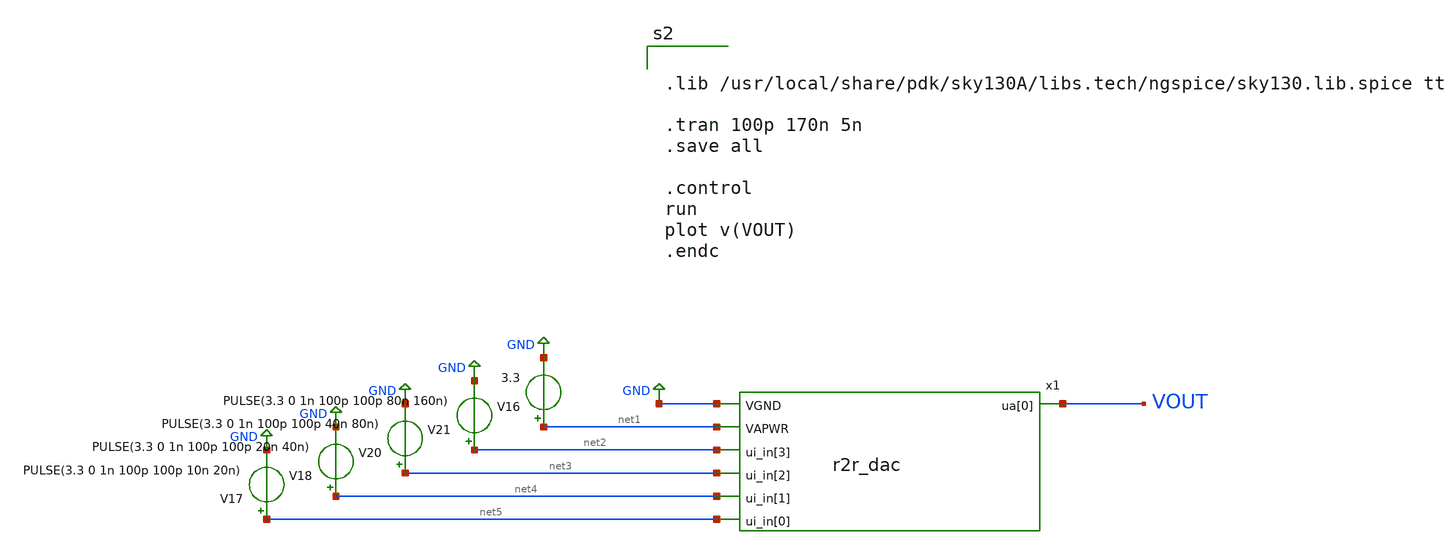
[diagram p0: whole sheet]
** sch_path: xschem/dac_tb.sch
**.subckt dac_tb
x1 VOUT GND net1 net2 net3 net4 net5 r2r_dac
V17 net5 GND PULSE(3.3 0 1n 100p 100p 10n 20n)
V18 net4 GND PULSE(3.3 0 1n 100p 100p 20n 40n)
V20 net3 GND PULSE(3.3 0 1n 100p 100p 40n 80n)
V21 net2 GND PULSE(3.3 0 1n 100p 100p 80n 160n)
V16 net1 GND 3.3
**** begin user architecture code


.lib /usr/local/share/pdk/sky130A/libs.tech/ngspice/sky130.lib.spice tt

.tran 100p 170n 5n
.save all

.control
run
plot v(VOUT)
.endc


**** end user architecture code
**.ends

* expanding   symbol:  /home/titus/TinyTapeout_R2R_DAC/xschem/r2r_dac.sym # of pins=7
** sym_path: xschem/r2r_dac.sym
** sch_path: xschem/r2r_dac.sch
.subckt r2r_dac ua[0] VGND VAPWR ui_in[3] ui_in[2] ui_in[1] ui_in[0]
*.opin ua[0]
*.ipin VGND
*.ipin ui_in[0]
*.ipin ui_in[1]
*.ipin ui_in[2]
*.ipin ui_in[3]
*.ipin VAPWR
XM10 net4 net5 VAPWR VAPWR sky130_fd_pr__pfet_g5v0d10v5 L=0.5 W=4 nf=1 ad=0 as=0 pd=0 ps=0 nrd=0
+ nrs=0 sa=0 sb=0 sd=0 mult=1 m=1
XM17 net4 ui_in[0] VGND VAPWR sky130_fd_pr__pfet_g5v0d10v5 L=0.5 W=4 nf=1 ad=0 as=0 pd=0 ps=0 nrd=0
+ nrs=0 sa=0 sb=0 sd=0 mult=1 m=1
XM26 net4 net5 VGND VGND sky130_fd_pr__nfet_g5v0d10v5 L=0.5 W=2 nf=1 ad=0 as=0 pd=0 ps=0 nrd=0 nrs=0
+ sa=0 sb=0 sd=0 mult=1 m=1
XM27 net4 ui_in[0] VAPWR VGND sky130_fd_pr__nfet_g5v0d10v5 L=0.5 W=2 nf=1 ad=0 as=0 pd=0 ps=0 nrd=0
+ nrs=0 sa=0 sb=0 sd=0 mult=1 m=1
XM32 net1 net6 VAPWR VAPWR sky130_fd_pr__pfet_g5v0d10v5 L=0.5 W=4 nf=1 ad=0 as=0 pd=0 ps=0 nrd=0
+ nrs=0 sa=0 sb=0 sd=0 mult=1 m=1
XM34 net1 ui_in[1] VGND VAPWR sky130_fd_pr__pfet_g5v0d10v5 L=0.5 W=4 nf=1 ad=0 as=0 pd=0 ps=0 nrd=0
+ nrs=0 sa=0 sb=0 sd=0 mult=1 m=1
XM1 net1 net6 VGND VGND sky130_fd_pr__nfet_g5v0d10v5 L=0.5 W=2 nf=1 ad=0 as=0 pd=0 ps=0 nrd=0 nrs=0
+ sa=0 sb=0 sd=0 mult=1 m=1
XM2 net1 ui_in[1] VAPWR VGND sky130_fd_pr__nfet_g5v0d10v5 L=0.5 W=2 nf=1 ad=0 as=0 pd=0 ps=0 nrd=0
+ nrs=0 sa=0 sb=0 sd=0 mult=1 m=1
XM4 net2 net7 VAPWR VAPWR sky130_fd_pr__pfet_g5v0d10v5 L=0.5 W=4 nf=1 ad=0 as=0 pd=0 ps=0 nrd=0
+ nrs=0 sa=0 sb=0 sd=0 mult=1 m=1
XM5 net2 ui_in[2] VGND VAPWR sky130_fd_pr__pfet_g5v0d10v5 L=0.5 W=4 nf=1 ad=0 as=0 pd=0 ps=0 nrd=0
+ nrs=0 sa=0 sb=0 sd=0 mult=1 m=1
XM8 net2 net7 VGND VGND sky130_fd_pr__nfet_g5v0d10v5 L=0.5 W=2 nf=1 ad=0 as=0 pd=0 ps=0 nrd=0 nrs=0
+ sa=0 sb=0 sd=0 mult=1 m=1
XM9 net2 ui_in[2] VAPWR VGND sky130_fd_pr__nfet_g5v0d10v5 L=0.5 W=2 nf=1 ad=0 as=0 pd=0 ps=0 nrd=0
+ nrs=0 sa=0 sb=0 sd=0 mult=1 m=1
XM11 net3 net8 VAPWR VAPWR sky130_fd_pr__pfet_g5v0d10v5 L=0.5 W=4 nf=1 ad=0 as=0 pd=0 ps=0 nrd=0
+ nrs=0 sa=0 sb=0 sd=0 mult=1 m=1
XM12 net3 ui_in[3] VGND VAPWR sky130_fd_pr__pfet_g5v0d10v5 L=0.5 W=4 nf=1 ad=0 as=0 pd=0 ps=0 nrd=0
+ nrs=0 sa=0 sb=0 sd=0 mult=1 m=1
XM15 net3 net8 VGND VGND sky130_fd_pr__nfet_g5v0d10v5 L=0.5 W=2 nf=1 ad=0 as=0 pd=0 ps=0 nrd=0 nrs=0
+ sa=0 sb=0 sd=0 mult=1 m=1
XM16 net3 ui_in[3] VAPWR VGND sky130_fd_pr__nfet_g5v0d10v5 L=0.5 W=2 nf=1 ad=0 as=0 pd=0 ps=0 nrd=0
+ nrs=0 sa=0 sb=0 sd=0 mult=1 m=1
XR10 B2 B1 VGND sky130_fd_pr__res_high_po_0p35 L=20 mult=1 m=1
XR9 B1 LSB VGND sky130_fd_pr__res_high_po_0p35 L=20 mult=1 m=1
XR11 ua[0] B2 VGND sky130_fd_pr__res_high_po_0p35 L=20 mult=1 m=1
XR12 LSB VGND VGND sky130_fd_pr__res_high_po_0p35 L=40 mult=1 m=1
XR13 net1 B1 VGND sky130_fd_pr__res_high_po_0p35 L=40 mult=1 m=1
XR14 net2 B2 VGND sky130_fd_pr__res_high_po_0p35 L=40 mult=1 m=1
XR15 net3 ua[0] VGND sky130_fd_pr__res_high_po_0p35 L=40 mult=1 m=1
XR3 net4 LSB VGND sky130_fd_pr__res_high_po_0p35 L=40 mult=1 m=1
**** begin user architecture code


.include /usr/local/share/pdk/sky130A/libs.ref/sky130_fd_sc_hvl/spice/sky130_fd_sc_hvl.spice


**** end user architecture code
x2 ui_in[0] VGND VGND VAPWR VAPWR net5 sky130_fd_sc_hvl__inv_1
x3 ui_in[1] VGND VGND VAPWR VAPWR net6 sky130_fd_sc_hvl__inv_1
x4 ui_in[2] VGND VGND VAPWR VAPWR net7 sky130_fd_sc_hvl__inv_1
x5 ui_in[3] VGND VGND VAPWR VAPWR net8 sky130_fd_sc_hvl__inv_1
.ends

.GLOBAL GND
.end
